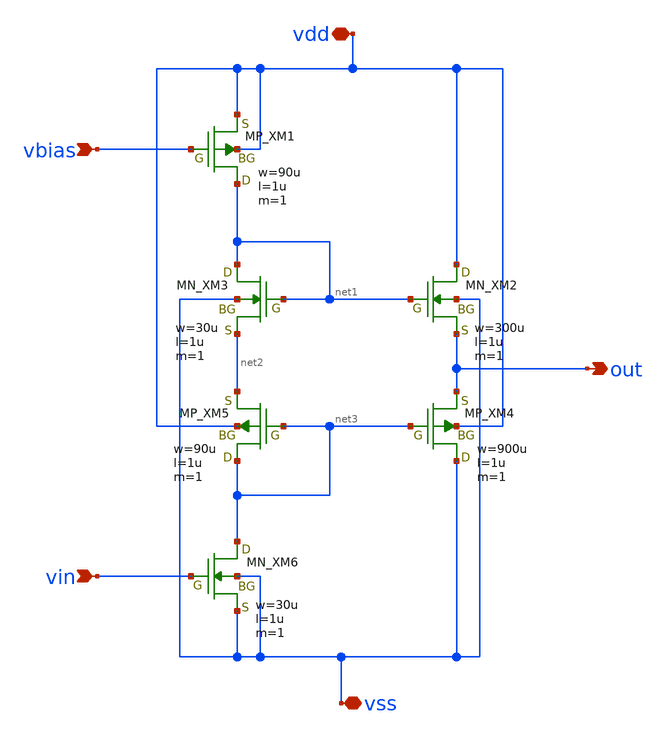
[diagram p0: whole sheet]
** sch_path: schematic/20250924_OSS_Workshop/ishikai/buf_pushpull/buf_pushpull.sch
**.subckt buf_pushpull out vin vss vdd vbias
*.opin out
*.ipin vin
*.iopin vss
*.iopin vdd
*.ipin vbias
XM1 net1 vbias vdd vdd PMOS w=90u l=1u as=0 ad=0 ps=0 pd=0 nrd=0 nrs=0 m=1
XM3 net1 net1 net2 vss NMOS w=30u l=1u as=0 ad=0 ps=0 pd=0 nrd=0 nrs=0 m=1
XM2 vdd net1 out vss NMOS w=300u l=1u as=0 ad=0 ps=0 pd=0 nrd=0 nrs=0 m=1
XM4 vss net3 out vdd PMOS w=900u l=1u as=0 ad=0 ps=0 pd=0 nrd=0 nrs=0 m=1
XM5 net3 net3 net2 vdd PMOS w=90u l=1u as=0 ad=0 ps=0 pd=0 nrd=0 nrs=0 m=1
XM6 net3 vin vss vss NMOS w=30u l=1u as=0 ad=0 ps=0 pd=0 nrd=0 nrs=0 m=1
**.ends
.end
